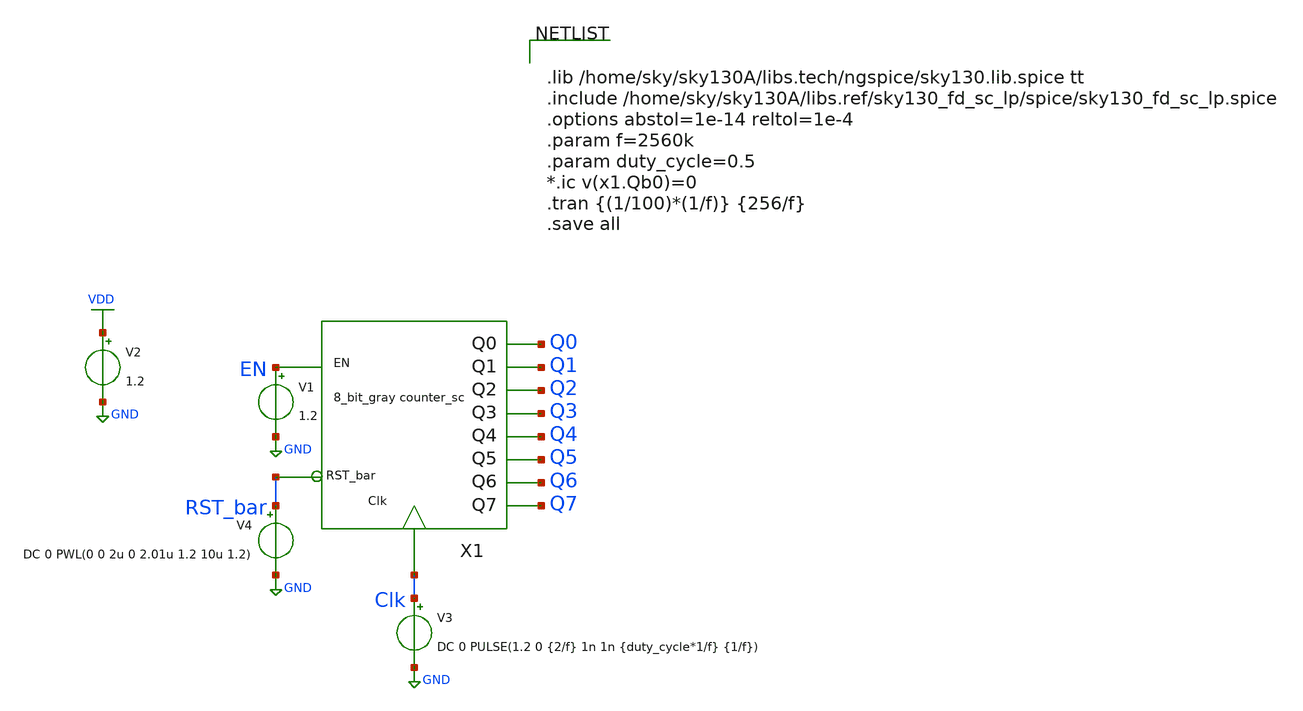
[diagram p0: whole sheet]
** sch_path: xschem/Asyn_rst_gray_counter/untitled-10.sch
**.subckt untitled-10
V3 Clk GND DC 0 PULSE(1.2 0 {2/f} 1n 1n {duty_cycle*1/f} {1/f})
V1 EN GND 1.2
V2 VDD GND 1.2
V4 RST_bar GND DC 0 PWL(0 0 2u 0 2.01u 1.2 10u 1.2)
X1 EN Q1 Q6 Clk Q0 Q2 Q3 Q4 Q5 Q7 RST_bar counter_8bit
**** begin user architecture code


.lib /home/sky/sky130A/libs.tech/ngspice/sky130.lib.spice tt
.include /home/sky/sky130A/libs.ref/sky130_fd_sc_lp/spice/sky130_fd_sc_lp.spice
.options abstol=1e-14 reltol=1e-4
.param f=2560k
.param duty_cycle=0.5
*.ic v(x1.Qb0)=0
.tran {(1/100)*(1/f)} {256/f}
.save all


**** end user architecture code
**.ends
.GLOBAL GND
.GLOBAL VDD
.end
